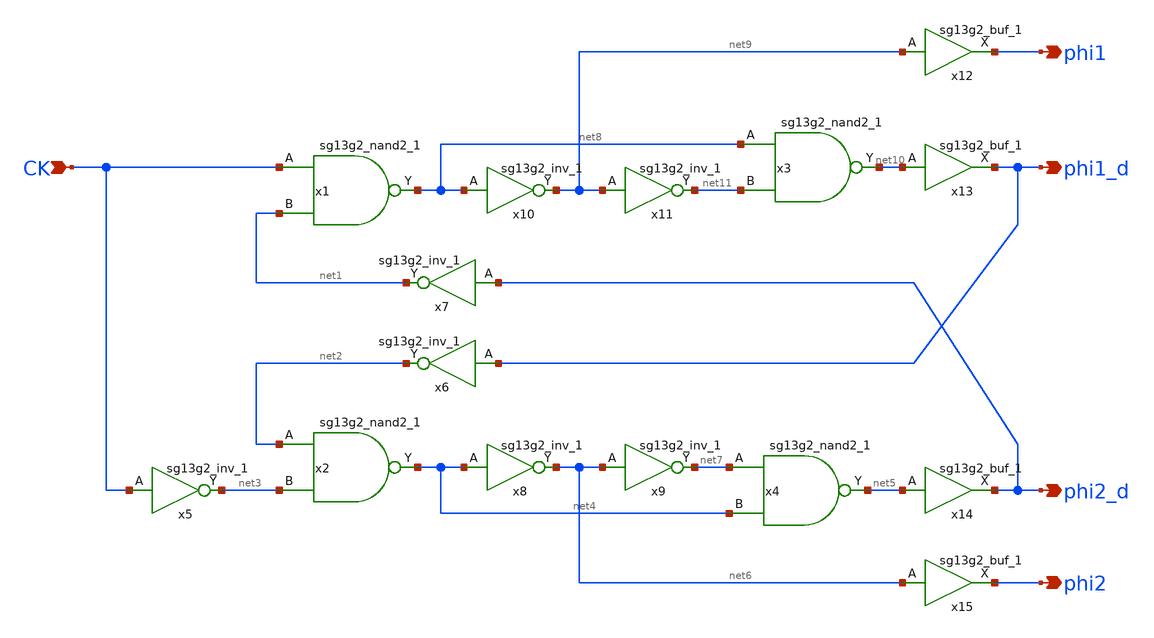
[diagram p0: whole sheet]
** sch_path: 3_real_circuits/clk_gen.sch
* IHP-GmbH/IHP-Open-PDK/ihp-sg13g2/libs.tech/xschem/sg13g2_stdcells/sg13g2_buf_1.sch:
* Copyright 2023 IHP PDK Authors
* Licensed under the Apache License, Version 2.0 (the "License");
**.subckt clk_gen CK phi1 phi1_d phi2_d phi2
*.ipin CK
*.opin phi1
*.opin phi1_d
*.opin phi2_d
*.opin phi2
x1 net8 CK net1 VDD VSS sg13g2_nand2_1
x2 net4 net2 net3 VDD VSS sg13g2_nand2_1
x3 net10 net8 net11 VDD VSS sg13g2_nand2_1
x4 net5 net7 net4 VDD VSS sg13g2_nand2_1
x5 net3 CK VDD VSS sg13g2_inv_1
x6 net2 phi1_d VDD VSS sg13g2_inv_1
x7 net1 phi2_d VDD VSS sg13g2_inv_1
x8 net6 net4 VDD VSS sg13g2_inv_1
x9 net7 net6 VDD VSS sg13g2_inv_1
x10 net9 net8 VDD VSS sg13g2_inv_1
x11 net11 net9 VDD VSS sg13g2_inv_1
x12 phi1 net9 VDD VSS sg13g2_buf_1
x13 phi1_d net10 VDD VSS sg13g2_buf_1
x14 phi2_d net5 VDD VSS sg13g2_buf_1
x15 phi2 net6 VDD VSS sg13g2_buf_1
**.ends

* expanding   symbol:  sg13g2_stdcells/sg13g2_nand2_1.sym # of pins=3
** sym_path: sg13g2_stdcells/sg13g2_nand2_1.sym
** sch_path: sg13g2_stdcells/sg13g2_nand2_1.sch
.subckt sg13g2_nand2_1 Y A B VDD VSS
*.iopin VDD
*.iopin VSS
*.ipin A
*.ipin B
*.opin Y
XM1 Y A net1 VSS sg13_lv_nmos w=740.00n l=130.00n ng=1 m=1 mm_ok=1
XM2 net1 B VSS VSS sg13_lv_nmos w=740.00n l=130.00n ng=1 m=1 mm_ok=1
XM3 Y A VDD VDD sg13_lv_pmos w=1.12u l=130.00n ng=1 m=1 mm_ok=1
XM4 Y B VDD VDD sg13_lv_pmos w=1.12u l=130.00n ng=1 m=1 mm_ok=1
.ends


* expanding   symbol:  sg13g2_stdcells/sg13g2_inv_1.sym # of pins=2
** sym_path: sg13g2_stdcells/sg13g2_inv_1.sym
** sch_path: sg13g2_stdcells/sg13g2_inv_1.sch
.subckt sg13g2_inv_1 Y A VDD VSS
*.opin Y
*.ipin A
*.iopin VDD
*.iopin VSS
XM1 Y A VSS VSS sg13_lv_nmos w=740.00n l=130.00n ng=1 m=1 mm_ok=1
XM2 Y A VDD VDD sg13_lv_pmos w=1.12u l=130.00n ng=1 m=1 mm_ok=1
.ends


* expanding   symbol:  sg13g2_stdcells/sg13g2_buf_1.sym # of pins=2
** sym_path: sg13g2_stdcells/sg13g2_buf_1.sym
** sch_path: sg13g2_stdcells/sg13g2_buf_1.sch
.subckt sg13g2_buf_1 X A VDD VSS
*.ipin A
*.opin X
*.iopin VDD
*.iopin VSS
XM1 net1 A VSS VSS sg13_lv_nmos w=550.00n l=130.00n ng=1 m=1 mm_ok=1
XM2 X net1 VSS VSS sg13_lv_nmos w=740.00n l=130.00n ng=1 m=1 mm_ok=1
XM3 net1 A VDD VDD sg13_lv_pmos w=840.00n l=130.00n ng=1 m=1 mm_ok=1
XM4 X net1 VDD VDD sg13_lv_pmos w=1.12u l=130.00n ng=1 m=1 mm_ok=1
.ends

.end
